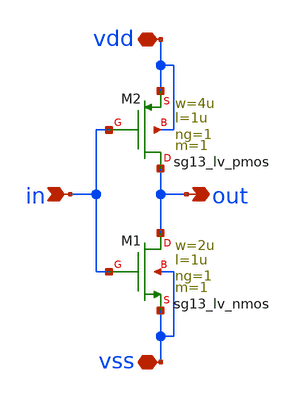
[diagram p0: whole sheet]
** sch_path: SSDOR_1.2V_v3/components/cgenerator/inv_ring_osc.sch
**.subckt inv_ring_osc vdd vss in out
*.iopin vdd
*.iopin vss
*.ipin in
*.opin out
XM1 out in vss vss sg13_lv_nmos w=2u l=1u ng=1 m=1 mm_ok=1
XM2 out in vdd vdd sg13_lv_pmos w=4u l=1u ng=1 m=1 mm_ok=1
**.ends
.end
